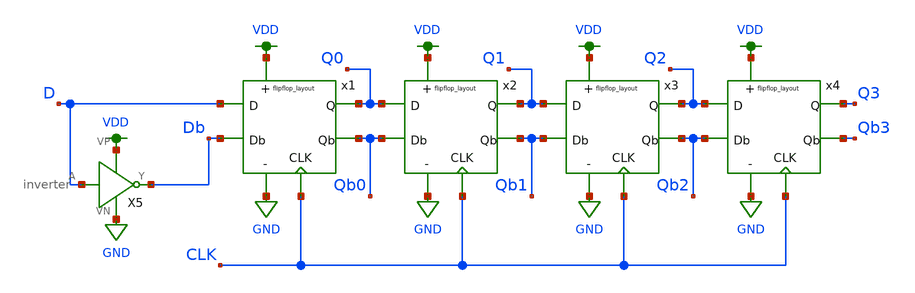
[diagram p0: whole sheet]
** sch_path: mp2/shiftreg.sch
**.subckt shiftreg
X5 D Db VDD GND inverter
x2 Q0 Q1 Qb0 Qb1 CLK VDD GND flipflop_layout
x3 Q1 Q2 Qb1 Qb2 CLK VDD GND flipflop_layout
x4 Q2 Q3 Qb2 Qb3 CLK VDD GND flipflop_layout
x1 D Q0 Db Qb0 CLK VDD GND flipflop_layout
**.ends

* expanding   symbol:  /home/jacob/documents/madvlsi/madvlsi-fa23/mp2/inverter.sym # of pins=4
** sym_path: mp2/inverter.sym
** sch_path: mp2/inverter.sch
.subckt inverter A Y VP VN
*.ipin A
*.opin Y
*.iopin VP
*.iopin VN
XM2 Y A VN VN sky130_fd_pr__nfet_01v8 L=0.15 W=1 nf=1 ad='int((nf+1)/2) * W/nf * 0.29' as='int((nf+2)/2) * W/nf * 0.29'
+ pd='2*int((nf+1)/2) * (W/nf + 0.29)' ps='2*int((nf+2)/2) * (W/nf + 0.29)' nrd='0.29 / W' nrs='0.29 / W'
+ sa=0 sb=0 sd=0 mult=1 m=1
XM1 Y A VP VP sky130_fd_pr__pfet_01v8 L=0.15 W=1 nf=1 ad='int((nf+1)/2) * W/nf * 0.29' as='int((nf+2)/2) * W/nf * 0.29'
+ pd='2*int((nf+1)/2) * (W/nf + 0.29)' ps='2*int((nf+2)/2) * (W/nf + 0.29)' nrd='0.29 / W' nrs='0.29 / W'
+ sa=0 sb=0 sd=0 mult=1 m=1
.ends


* expanding   symbol:  /home/jacob/madvlsi-fa23/mp2/flipflop_layout.sym # of pins=7
** sym_path: mp2/flipflop_layout.sym
** sch_path: mp2/flipflop_layout.sch
.subckt flipflop_layout D Q Db Qb CLK VP VN
*.ipin D
*.ipin Db
*.ipin CLK
*.opin Q
*.opin Qb
*.iopin VP
*.iopin VN
XM1 net2 CLK D VDD sky130_fd_pr__pfet_01v8 L=0.15 W=1 nf=1 ad='int((nf+1)/2) * W/nf * 0.29' as='int((nf+2)/2) * W/nf * 0.29'
+ pd='2*int((nf+1)/2) * (W/nf + 0.29)' ps='2*int((nf+2)/2) * (W/nf + 0.29)' nrd='0.29 / W' nrs='0.29 / W'
+ sa=0 sb=0 sd=0 mult=1 m=1
XM2 net3 CLK Db VDD sky130_fd_pr__pfet_01v8 L=0.15 W=1 nf=1 ad='int((nf+1)/2) * W/nf * 0.29' as='int((nf+2)/2) * W/nf * 0.29'
+ pd='2*int((nf+1)/2) * (W/nf + 0.29)' ps='2*int((nf+2)/2) * (W/nf + 0.29)' nrd='0.29 / W' nrs='0.29 / W'
+ sa=0 sb=0 sd=0 mult=1 m=1
XM3 net2 CLK Q GND sky130_fd_pr__nfet_01v8 L=0.15 W=1 nf=1 ad='int((nf+1)/2) * W/nf * 0.29' as='int((nf+2)/2) * W/nf * 0.29'
+ pd='2*int((nf+1)/2) * (W/nf + 0.29)' ps='2*int((nf+2)/2) * (W/nf + 0.29)' nrd='0.29 / W' nrs='0.29 / W'
+ sa=0 sb=0 sd=0 mult=1 m=1
XM4 net3 CLK Qb GND sky130_fd_pr__nfet_01v8 L=0.15 W=1 nf=1 ad='int((nf+1)/2) * W/nf * 0.29' as='int((nf+2)/2) * W/nf * 0.29'
+ pd='2*int((nf+1)/2) * (W/nf + 0.29)' ps='2*int((nf+2)/2) * (W/nf + 0.29)' nrd='0.29 / W' nrs='0.29 / W'
+ sa=0 sb=0 sd=0 mult=1 m=1
XM5 VN CLK net1 GND sky130_fd_pr__nfet_01v8 L=0.15 W=3.85 nf=1 ad='int((nf+1)/2) * W/nf * 0.29' as='int((nf+2)/2) * W/nf * 0.29'
+ pd='2*int((nf+1)/2) * (W/nf + 0.29)' ps='2*int((nf+2)/2) * (W/nf + 0.29)' nrd='0.29 / W' nrs='0.29 / W'
+ sa=0 sb=0 sd=0 mult=1 m=1
XM6 net1 net2 net3 GND sky130_fd_pr__nfet_01v8 L=0.15 W=1 nf=1 ad='int((nf+1)/2) * W/nf * 0.29' as='int((nf+2)/2) * W/nf * 0.29'
+ pd='2*int((nf+1)/2) * (W/nf + 0.29)' ps='2*int((nf+2)/2) * (W/nf + 0.29)' nrd='0.29 / W' nrs='0.29 / W'
+ sa=0 sb=0 sd=0 mult=1 m=1
XM7 net1 net3 net2 GND sky130_fd_pr__nfet_01v8 L=0.15 W=1 nf=1 ad='int((nf+1)/2) * W/nf * 0.29' as='int((nf+2)/2) * W/nf * 0.29'
+ pd='2*int((nf+1)/2) * (W/nf + 0.29)' ps='2*int((nf+2)/2) * (W/nf + 0.29)' nrd='0.29 / W' nrs='0.29 / W'
+ sa=0 sb=0 sd=0 mult=1 m=1
XM8 VP net2 net3 VDD sky130_fd_pr__pfet_01v8 L=0.15 W=1 nf=1 ad='int((nf+1)/2) * W/nf * 0.29' as='int((nf+2)/2) * W/nf * 0.29'
+ pd='2*int((nf+1)/2) * (W/nf + 0.29)' ps='2*int((nf+2)/2) * (W/nf + 0.29)' nrd='0.29 / W' nrs='0.29 / W'
+ sa=0 sb=0 sd=0 mult=1 m=1
XM9 VP net3 net2 VDD sky130_fd_pr__pfet_01v8 L=0.15 W=1 nf=1 ad='int((nf+1)/2) * W/nf * 0.29' as='int((nf+2)/2) * W/nf * 0.29'
+ pd='2*int((nf+1)/2) * (W/nf + 0.29)' ps='2*int((nf+2)/2) * (W/nf + 0.29)' nrd='0.29 / W' nrs='0.29 / W'
+ sa=0 sb=0 sd=0 mult=1 m=1
XM10 net4 CLK VP VDD sky130_fd_pr__pfet_01v8 L=0.15 W=3.85 nf=1 ad='int((nf+1)/2) * W/nf * 0.29' as='int((nf+2)/2) * W/nf * 0.29'
+ pd='2*int((nf+1)/2) * (W/nf + 0.29)' ps='2*int((nf+2)/2) * (W/nf + 0.29)' nrd='0.29 / W' nrs='0.29 / W'
+ sa=0 sb=0 sd=0 mult=1 m=1
XM11 Qb Q net4 VDD sky130_fd_pr__pfet_01v8 L=0.15 W=1 nf=1 ad='int((nf+1)/2) * W/nf * 0.29' as='int((nf+2)/2) * W/nf * 0.29'
+ pd='2*int((nf+1)/2) * (W/nf + 0.29)' ps='2*int((nf+2)/2) * (W/nf + 0.29)' nrd='0.29 / W' nrs='0.29 / W'
+ sa=0 sb=0 sd=0 mult=1 m=1
XM12 Q Qb net4 VDD sky130_fd_pr__pfet_01v8 L=0.15 W=1 nf=1 ad='int((nf+1)/2) * W/nf * 0.29' as='int((nf+2)/2) * W/nf * 0.29'
+ pd='2*int((nf+1)/2) * (W/nf + 0.29)' ps='2*int((nf+2)/2) * (W/nf + 0.29)' nrd='0.29 / W' nrs='0.29 / W'
+ sa=0 sb=0 sd=0 mult=1 m=1
XM13 VN Q Qb GND sky130_fd_pr__nfet_01v8 L=0.15 W=1 nf=1 ad='int((nf+1)/2) * W/nf * 0.29' as='int((nf+2)/2) * W/nf * 0.29'
+ pd='2*int((nf+1)/2) * (W/nf + 0.29)' ps='2*int((nf+2)/2) * (W/nf + 0.29)' nrd='0.29 / W' nrs='0.29 / W'
+ sa=0 sb=0 sd=0 mult=1 m=1
XM14 VN Qb Q GND sky130_fd_pr__nfet_01v8 L=0.15 W=1 nf=1 ad='int((nf+1)/2) * W/nf * 0.29' as='int((nf+2)/2) * W/nf * 0.29'
+ pd='2*int((nf+1)/2) * (W/nf + 0.29)' ps='2*int((nf+2)/2) * (W/nf + 0.29)' nrd='0.29 / W' nrs='0.29 / W'
+ sa=0 sb=0 sd=0 mult=1 m=1
.ends

.GLOBAL VDD
.GLOBAL GND
.end
